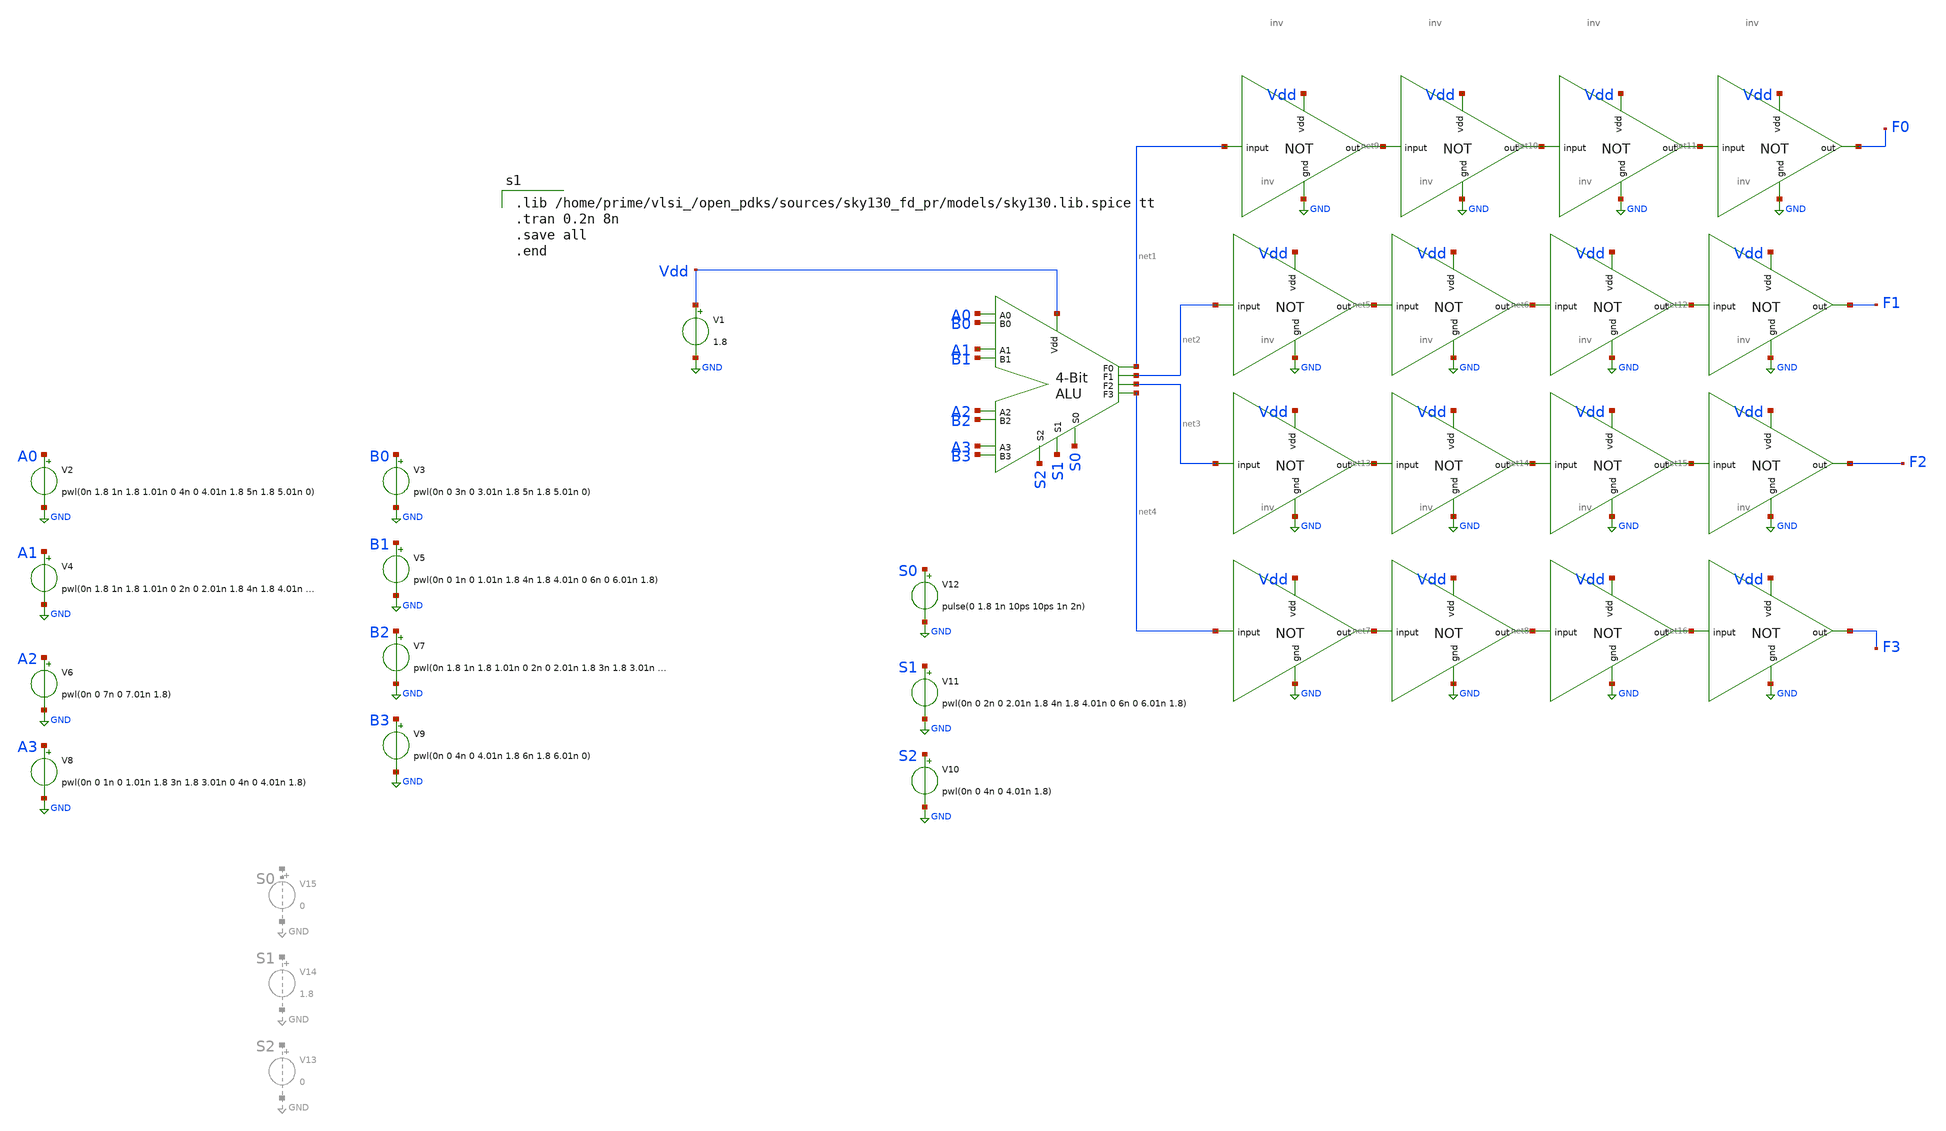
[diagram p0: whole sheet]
** sch_path: extra_stuff/top_bk.sch
**.subckt top_bk
x1 net1 net2 net3 net4 Vdd A0 B0 A1 B1 A2 B2 A3 B3 S0 S1 S2 alu
V1 Vdd GND 1.8
V2 A0 GND pwl(0n 1.8 1n 1.8 1.01n 0 4n 0 4.01n 1.8 5n 1.8 5.01n 0)
V3 B0 GND pwl(0n 0 3n 0 3.01n 1.8 5n 1.8 5.01n 0)
V4 A1 GND pwl(0n 1.8 1n 1.8 1.01n 0 2n 0 2.01n 1.8 4n 1.8 4.01n 0 6n 0 6.01n 1.8 7n 1.8 7.01n 0)
V5 B1 GND pwl(0n 0 1n 0 1.01n 1.8 4n 1.8 4.01n 0 6n 0 6.01n 1.8)
V6 A2 GND pwl(0n 0 7n 0 7.01n 1.8)
V7 B2 GND pwl(0n 1.8 1n 1.8 1.01n 0 2n 0 2.01n 1.8 3n 1.8 3.01n 0 4n 0 4.01n 1.8 5n 1.8 5.01n 0 6n 0
+ 6.01n 1.8)
V8 A3 GND pwl(0n 0 1n 0 1.01n 1.8 3n 1.8 3.01n 0 4n 0 4.01n 1.8)
V9 B3 GND pwl(0n 0 4n 0 4.01n 1.8 6n 1.8 6.01n 0)
V10 S2 GND pwl(0n 0 4n 0 4.01n 1.8)
V11 S1 GND pwl(0n 0 2n 0 2.01n 1.8 4n 1.8 4.01n 0 6n 0 6.01n 1.8)
V12 S0 GND pulse(0 1.8 1n 10ps 10ps 1n 2n)
x4 net5 Vdd net2 GND inv
x5 net6 Vdd net5 GND inv
x8 net7 Vdd net4 GND inv
x9 net8 Vdd net7 GND inv
x3 net9 Vdd net1 GND inv
x6 net10 Vdd net9 GND inv
x7 net11 Vdd net10 GND inv
x16 F0 Vdd net11 GND inv
x17 net12 Vdd net6 GND inv
x18 F1 Vdd net12 GND inv
x2 net13 Vdd net3 GND inv
x19 net14 Vdd net13 GND inv
x20 net15 Vdd net14 GND inv
x21 F2 Vdd net15 GND inv
x22 net16 Vdd net8 GND inv
x23 F3 Vdd net16 GND inv
**** begin user architecture code

.lib /home/prime/vlsi_/open_pdks/sources/sky130_fd_pr/models/sky130.lib.spice tt
.tran 0.2n 8n
.save all
.end

**** end user architecture code
**.ends
.GLOBAL GND
.end
